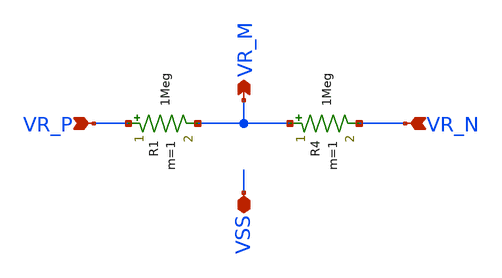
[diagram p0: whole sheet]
** sch_path: macros/filter_cmos5l/schematic/xschem/rstring_cm.sch
**.subckt rstring_cm VSS VR_P VR_N VR_M
*.iopin VSS
*.ipin VR_P
*.ipin VR_N
*.opin VR_M
R1 VR_P VR_M 1Meg m=1
R4 VR_M VR_N 1Meg m=1
**.ends
.end
